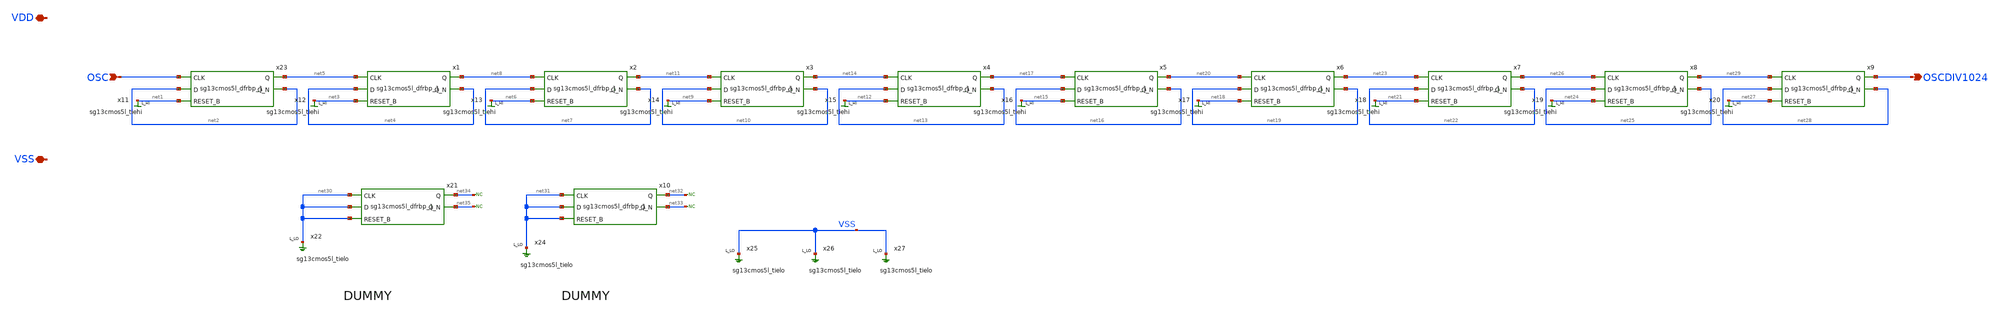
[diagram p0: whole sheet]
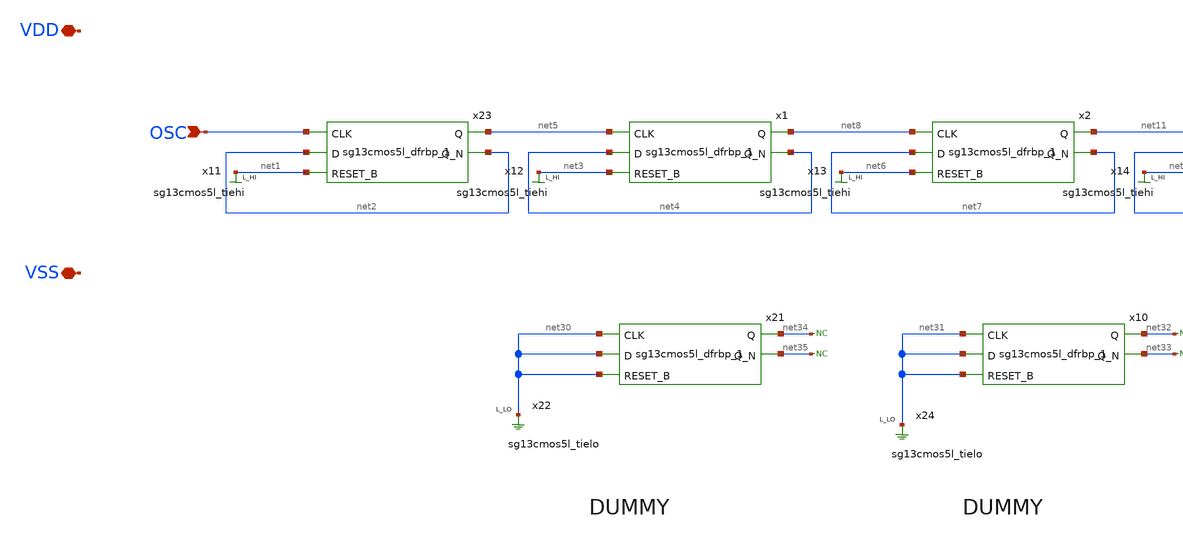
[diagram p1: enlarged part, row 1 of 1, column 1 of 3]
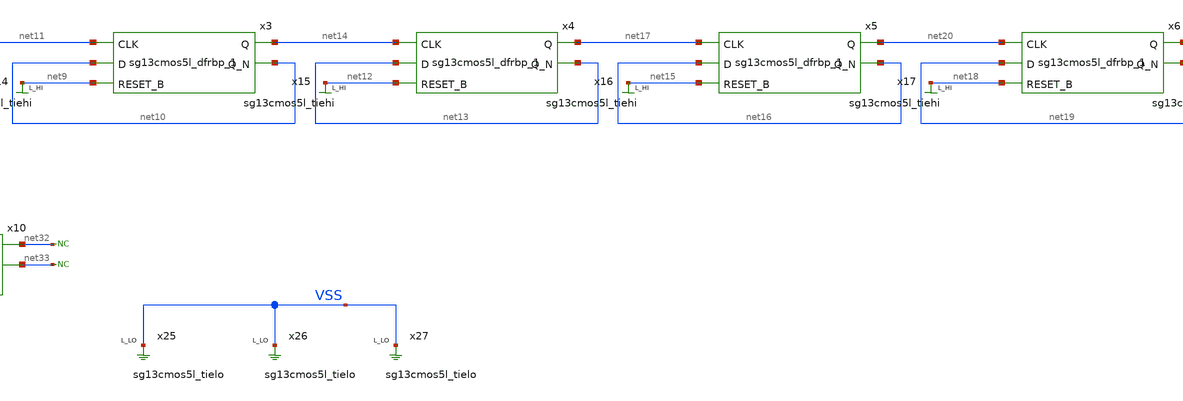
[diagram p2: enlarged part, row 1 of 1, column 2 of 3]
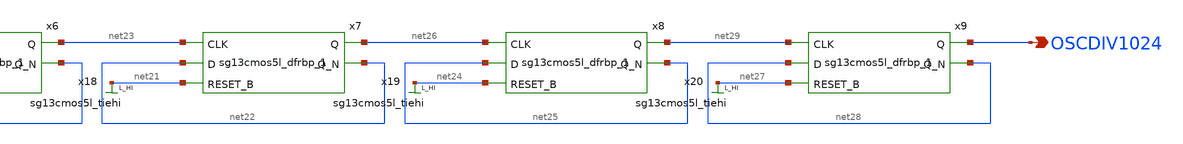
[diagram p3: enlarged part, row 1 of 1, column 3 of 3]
** sch_path: MPU9547-main/analog/schematic/DIV1024.sch
**.subckt DIV1024 VDD VSS OSC OSCDIV1024
*.iopin VDD
*.iopin VSS
*.ipin OSC
*.opin OSCDIV1024
x23 net5 net2 OSC net2 net1 VDD VSS sg13cmos5l_dfrbp_1
x1 net8 net4 net5 net4 net3 VDD VSS sg13cmos5l_dfrbp_1
x2 net11 net7 net8 net7 net6 VDD VSS sg13cmos5l_dfrbp_1
x3 net14 net10 net11 net10 net9 VDD VSS sg13cmos5l_dfrbp_1
x4 net17 net13 net14 net13 net12 VDD VSS sg13cmos5l_dfrbp_1
x5 net20 net16 net17 net16 net15 VDD VSS sg13cmos5l_dfrbp_1
x6 net23 net19 net20 net19 net18 VDD VSS sg13cmos5l_dfrbp_1
x7 net26 net22 net23 net22 net21 VDD VSS sg13cmos5l_dfrbp_1
x8 net29 net25 net26 net25 net24 VDD VSS sg13cmos5l_dfrbp_1
x9 OSCDIV1024 net28 net29 net28 net27 VDD VSS sg13cmos5l_dfrbp_1
x11 net1 VDD VSS sg13cmos5l_tiehi
x12 net3 VDD VSS sg13cmos5l_tiehi
x13 net6 VDD VSS sg13cmos5l_tiehi
x14 net9 VDD VSS sg13cmos5l_tiehi
x15 net12 VDD VSS sg13cmos5l_tiehi
x16 net15 VDD VSS sg13cmos5l_tiehi
x17 net18 VDD VSS sg13cmos5l_tiehi
x18 net21 VDD VSS sg13cmos5l_tiehi
x19 net24 VDD VSS sg13cmos5l_tiehi
x20 net27 VDD VSS sg13cmos5l_tiehi
x10 net32 net33 net31 net31 net31 VDD VSS sg13cmos5l_dfrbp_1
x21 net34 net35 net30 net30 net30 VDD VSS sg13cmos5l_dfrbp_1
x22 net30 VDD VSS sg13cmos5l_tielo
x24 net31 VDD VSS sg13cmos5l_tielo
* noconn #net34
* noconn #net35
* noconn #net32
* noconn #net33
x25 VSS VDD VSS sg13cmos5l_tielo
x26 VSS VDD VSS sg13cmos5l_tielo
x27 VSS VDD VSS sg13cmos5l_tielo
**.ends
.end
